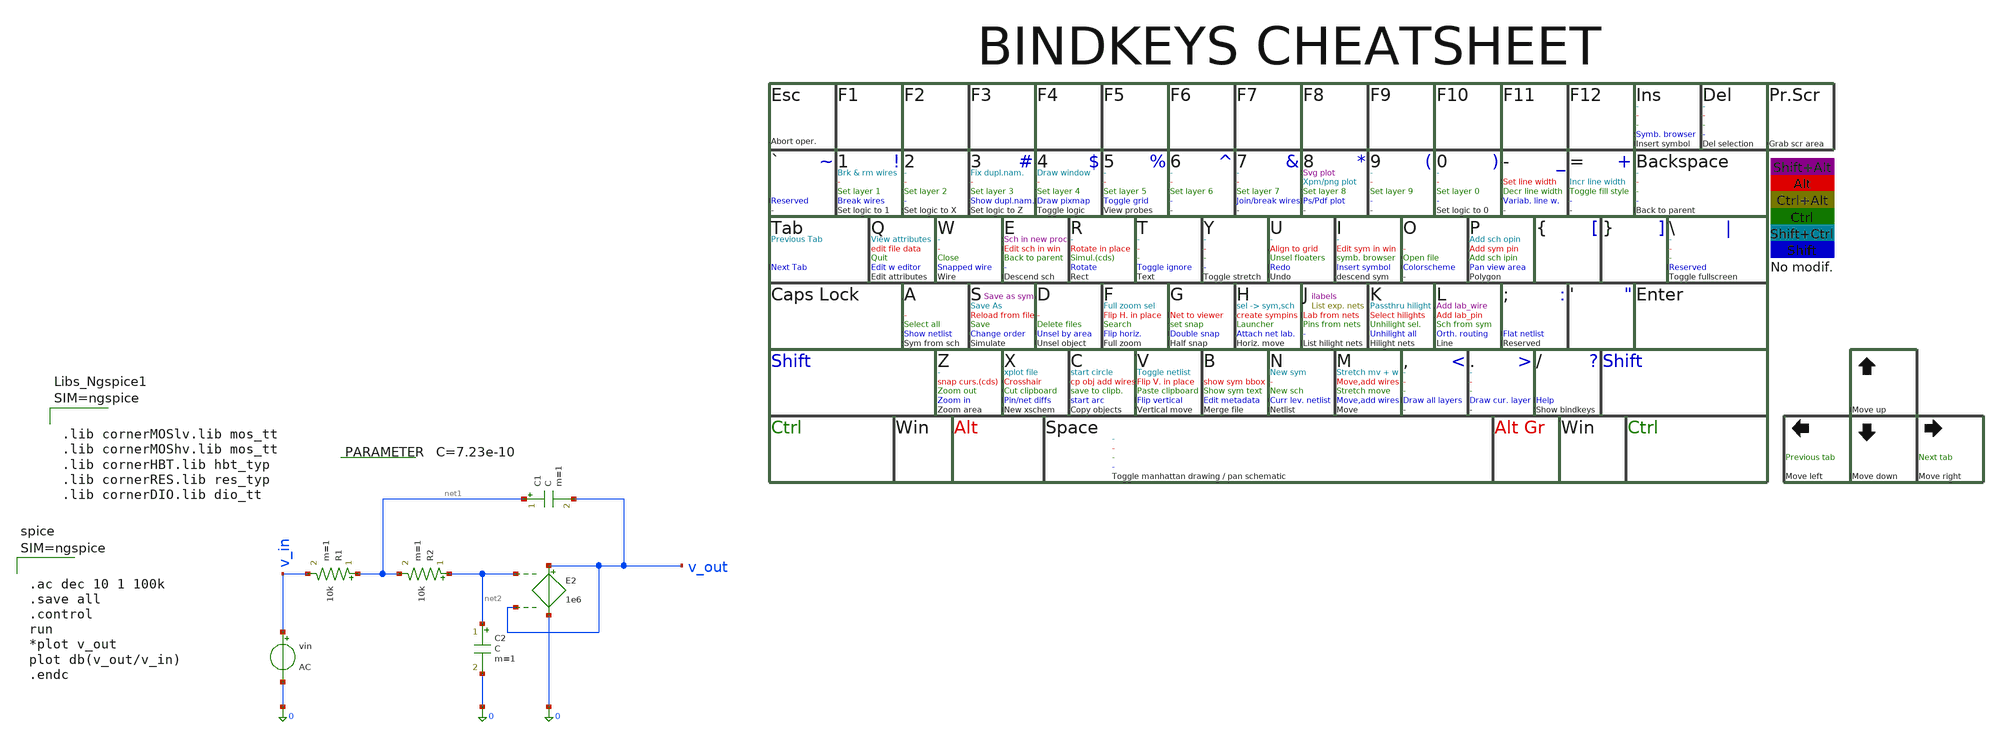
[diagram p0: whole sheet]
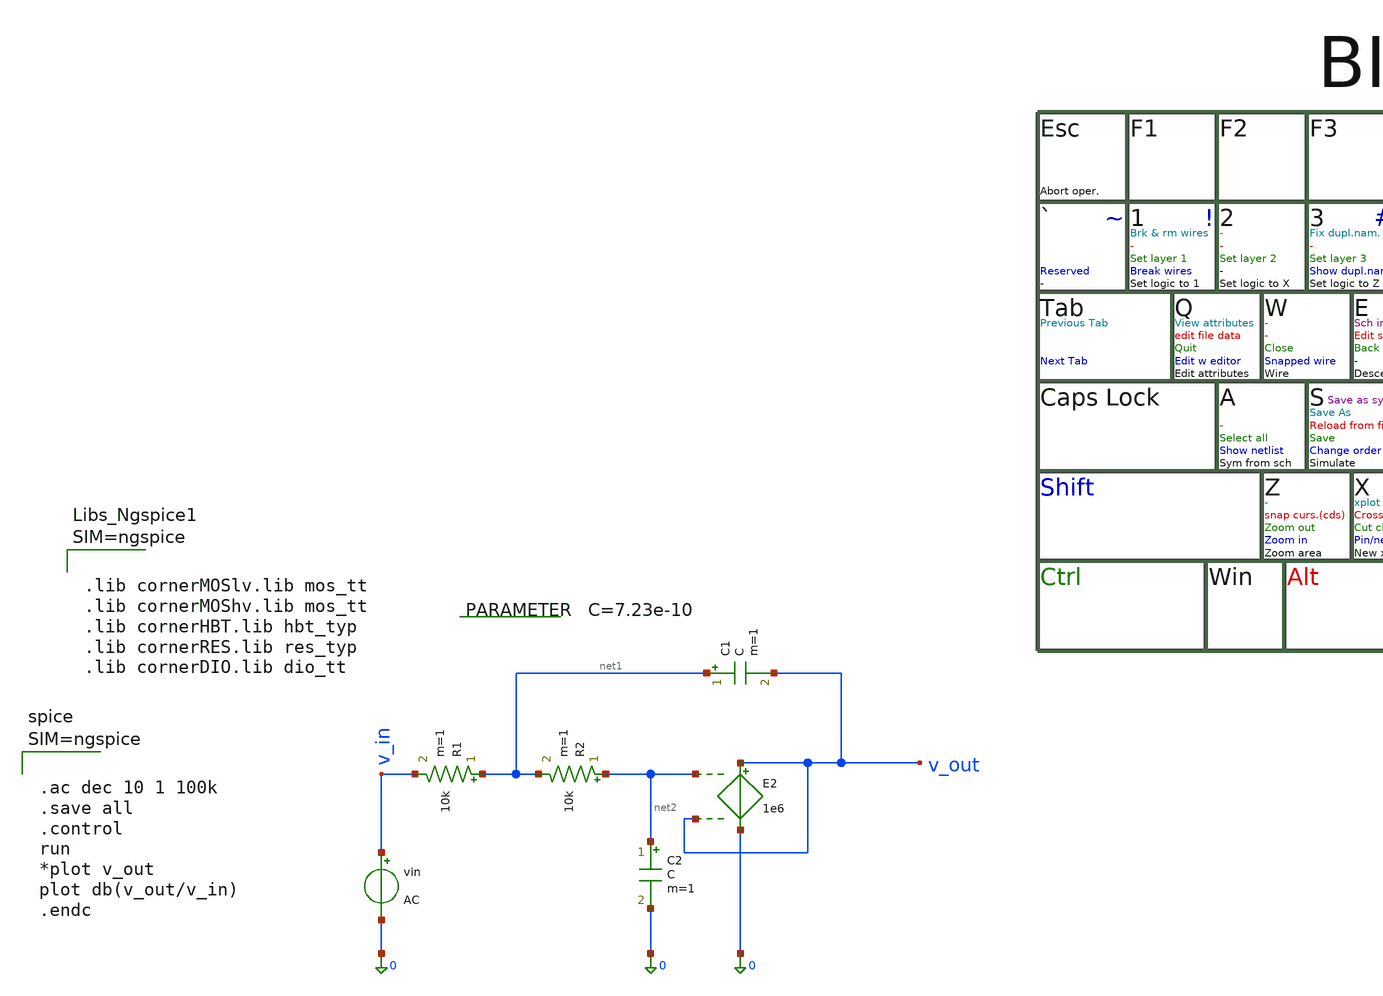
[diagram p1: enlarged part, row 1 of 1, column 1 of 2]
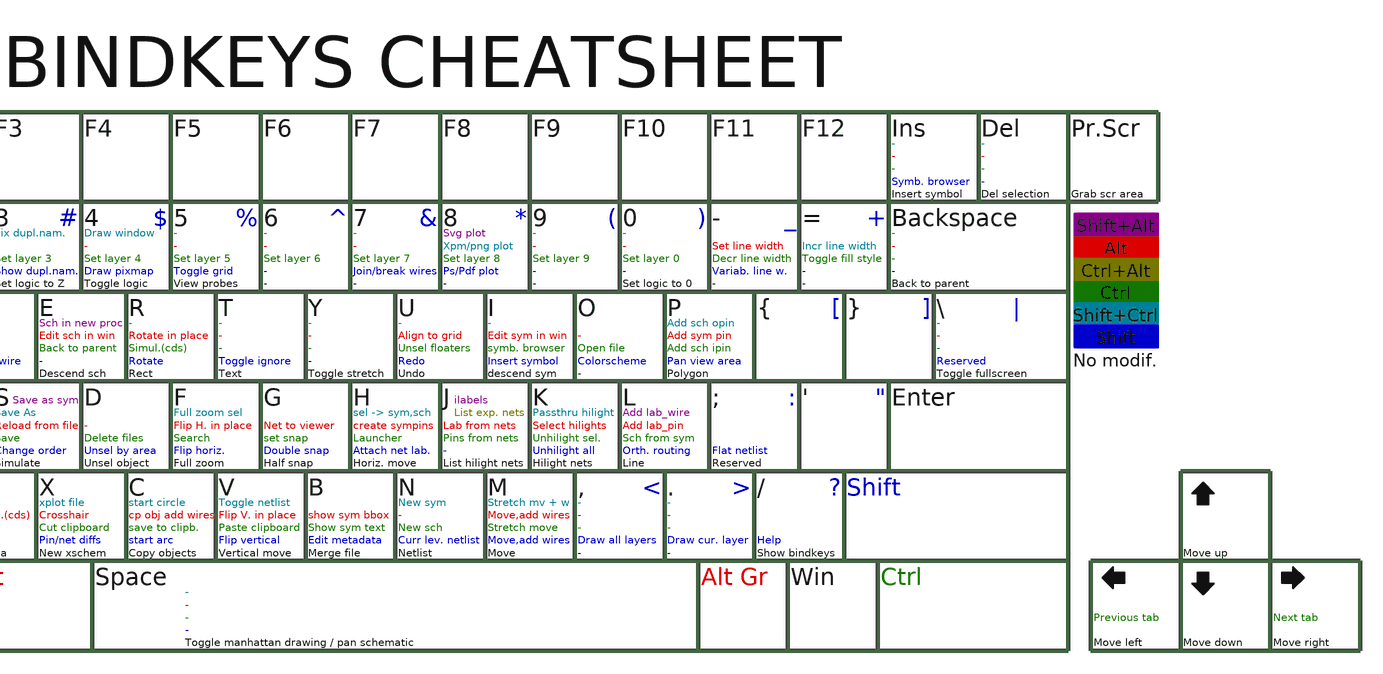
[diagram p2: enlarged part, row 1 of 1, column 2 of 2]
** sch_path: 001_Design/Ideal_Circuits/sallen_key_ac.sch
**.subckt sallen_key_ac
R1 net1 v_in 10k m=1
R2 net2 net1 10k m=1
C1 net1 v_out C m=1
C2 net2 0 C m=1
E2 v_out 0 net2 v_out 1e6
vin v_in 0 AC
.param C=7.23e-10
**** begin user architecture code



.lib cornerMOSlv.lib mos_tt
.lib cornerMOShv.lib mos_tt
.lib cornerHBT.lib hbt_typ
.lib cornerRES.lib res_typ
.lib cornerDIO.lib dio_tt






.ac dec 10 1 100k
.save all
.control
run
*plot v_out
plot db(v_out/v_in)
.endc



**** end user architecture code
**.ends
.end
